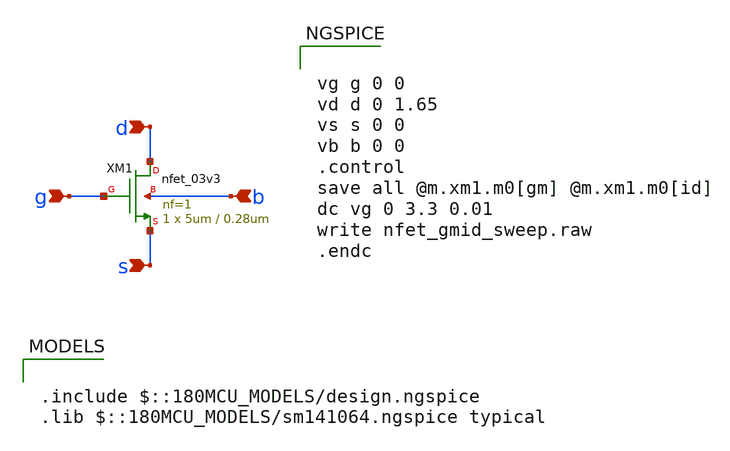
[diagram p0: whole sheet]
** sch_path: designs/single_nfet_test.sch
* Copyright 2022 GlobalFoundries PDK Authors
* Licensed under the Apache License, Version 2.0 (the "License");
* you may not use this file except in compliance with the License.
* You may obtain a copy of the License at
* https://www.apache.org/licenses/LICENSE-2.0
* Unless required by applicable law or agreed to in writing, software
* distributed under the License is distributed on an "AS IS" BASIS,
* WITHOUT WARRANTIES OR CONDITIONS OF ANY KIND, either express or implied.
* See the License for the specific language governing permissions and
* limitations under the License.
**.subckt single_nfet_test d s g b
*.ipin d
*.ipin s
*.ipin g
*.ipin b
XM1 d g s b nfet_03v3 L=0.28um W=5um nf=1 ad='int((nf+1)/2) * W/nf * 0.18u' as='int((nf+2)/2) * W/nf * 0.18u'
+ pd='2*int((nf+1)/2) * (W/nf + 0.18u)' ps='2*int((nf+2)/2) * (W/nf + 0.18u)' nrd='0.18u / W' nrs='0.18u / W'
+ sa=0 sb=0 sd=0 m=1
**** begin user architecture code

.include $::180MCU_MODELS/design.ngspice
.lib $::180MCU_MODELS/sm141064.ngspice typical



vg g 0 0
vd d 0 1.65
vs s 0 0
vb b 0 0
.control
save all @m.xm1.m0[gm] @m.xm1.m0[id]
dc vg 0 3.3 0.01
write nfet_gmid_sweep.raw
.endc


**** end user architecture code
**.ends
.end
